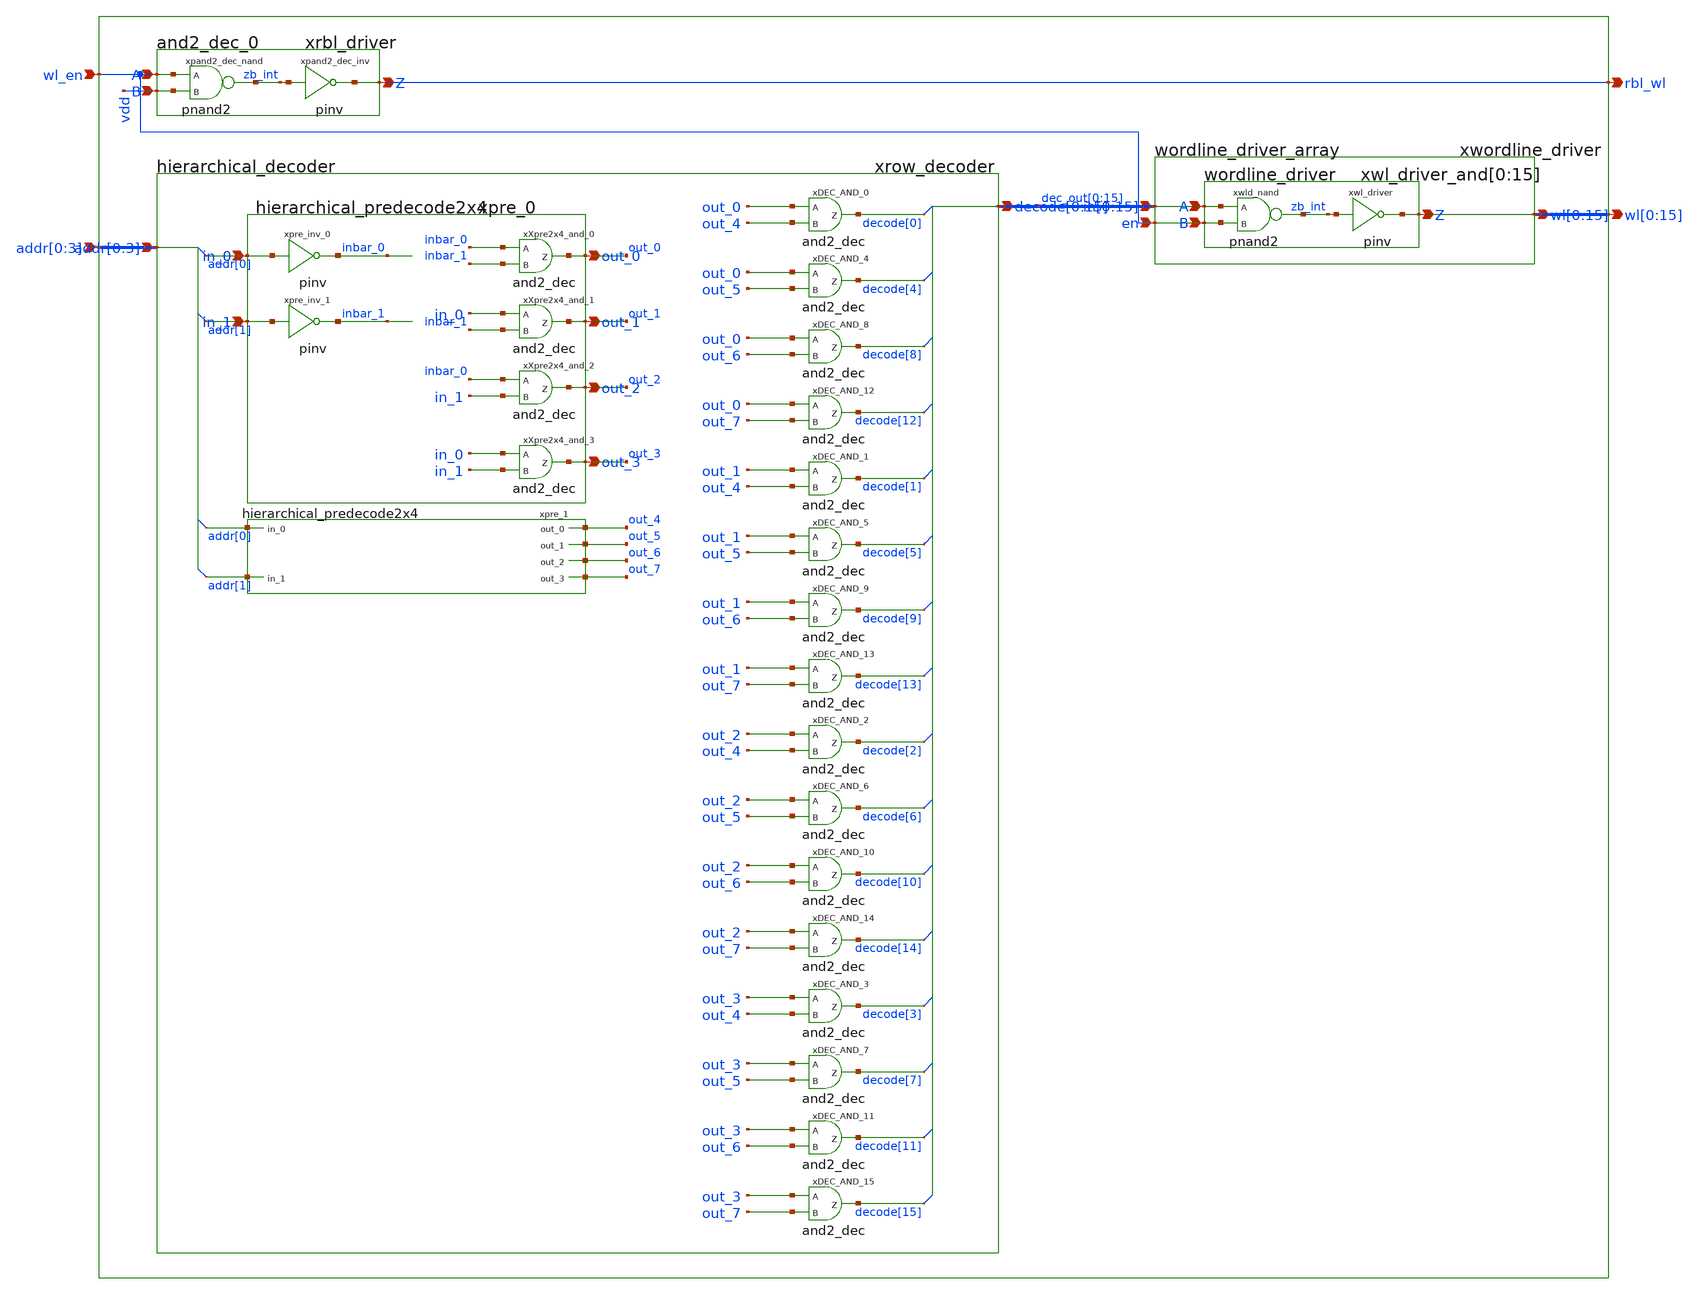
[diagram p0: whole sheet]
** sch_path: sram_4_16_scn4m/port_address.sch
**.subckt port_address addr[0],addr[1],addr[2],addr[3] wl_en
*+ wl[0],wl[1],wl[2],wl[3],wl[4],wl[5],wl[6],wl[7],wl[8],wl[9],wl[10],wl[11],wl[12],wl[13],wl[14],wl[15] rbl_wl
*.ipin addr[0],addr[1],addr[2],addr[3]
*.ipin wl_en
*.opin
*+ wl[0],wl[1],wl[2],wl[3],wl[4],wl[5],wl[6],wl[7],wl[8],wl[9],wl[10],wl[11],wl[12],wl[13],wl[14],wl[15]
*.opin rbl_wl
xrow_decoder addr[0] addr[1] addr[2] addr[3] dec_out[0] dec_out[1] dec_out[2] dec_out[3] dec_out[4]
+ dec_out[5] dec_out[6] dec_out[7] dec_out[8] dec_out[9] dec_out[10] dec_out[11] dec_out[12] dec_out[13]
+ dec_out[14] dec_out[15] vdd gnd hierarchical_decoder
xwordline_driver dec_out[0] dec_out[1] dec_out[2] dec_out[3] dec_out[4] dec_out[5] dec_out[6]
+ dec_out[7] dec_out[8] dec_out[9] dec_out[10] dec_out[11] dec_out[12] dec_out[13] dec_out[14] dec_out[15] wl[0]
+ wl[1] wl[2] wl[3] wl[4] wl[5] wl[6] wl[7] wl[8] wl[9] wl[10] wl[11] wl[12] wl[13] wl[14] wl[15] wl_en vdd
+ gnd wordline_driver_array
xrbl_driver wl_en vdd rbl_wl vdd gnd and2_dec_0
**.ends

* expanding   symbol:  hierarchical_decoder.sch # of pins=2
** sym_path: sram_4_16_scn4m/hierarchical_decoder.sch
** sch_path: sram_4_16_scn4m/hierarchical_decoder.sch
.subckt hierarchical_decoder addr[0] addr[1] addr[2] addr[3] decode[0] decode[1] decode[2] decode[3]
+ decode[4] decode[5] decode[6] decode[7] decode[8] decode[9] decode[10] decode[11] decode[12] decode[13]
+ decode[14] decode[15] vdd gnd
*.ipin addr[0],addr[1],addr[2],addr[3]
*.opin
*+ decode[0],decode[1],decode[2],decode[3],decode[4],decode[5],decode[6],decode[7],decode[8],decode[9],decode[10],decode[11],decode[12],decode[13],decode[14],decode[15]
xpre_0 addr[0] addr[1] out_0 out_1 out_2 out_3 vdd gnd hierarchical_predecode2x4
xpre_1 addr[0] addr[1] out_4 out_5 out_6 out_7 vdd gnd hierarchical_predecode2x4
xDEC_AND_0 out_0 out_4 decode[0] and2_dec
xDEC_AND_4 out_0 out_5 decode[4] and2_dec
xDEC_AND_8 out_0 out_6 decode[8] and2_dec
xDEC_AND_12 out_0 out_7 decode[12] and2_dec
xDEC_AND_1 out_1 out_4 decode[1] and2_dec
xDEC_AND_5 out_1 out_5 decode[5] and2_dec
xDEC_AND_9 out_1 out_6 decode[9] and2_dec
xDEC_AND_13 out_1 out_7 decode[13] and2_dec
xDEC_AND_2 out_2 out_4 decode[2] and2_dec
xDEC_AND_6 out_2 out_5 decode[6] and2_dec
xDEC_AND_10 out_2 out_6 decode[10] and2_dec
xDEC_AND_14 out_2 out_7 decode[14] and2_dec
xDEC_AND_3 out_3 out_4 decode[3] and2_dec
xDEC_AND_7 out_3 out_5 decode[7] and2_dec
xDEC_AND_11 out_3 out_6 decode[11] and2_dec
xDEC_AND_15 out_3 out_7 decode[15] and2_dec
.ends


* expanding   symbol:  wordline_driver_array.sch # of pins=3
** sym_path: sram_4_16_scn4m/wordline_driver_array.sch
** sch_path: sram_4_16_scn4m/wordline_driver_array.sch
.subckt wordline_driver_array in[0] in[1] in[2] in[3] in[4] in[5] in[6] in[7] in[8] in[9] in[10]
+ in[11] in[12] in[13] in[14] in[15] wl[0] wl[1] wl[2] wl[3] wl[4] wl[5] wl[6] wl[7] wl[8] wl[9] wl[10]
+ wl[11] wl[12] wl[13] wl[14] wl[15] en vdd gnd
*.ipin
*+ in[0],in[1],in[2],in[3],in[4],in[5],in[6],in[7],in[8],in[9],in[10],in[11],in[12],in[13],in[14],in[15]
*.opin
*+ wl[0],wl[1],wl[2],wl[3],wl[4],wl[5],wl[6],wl[7],wl[8],wl[9],wl[10],wl[11],wl[12],wl[13],wl[14],wl[15]
*.ipin en
xwl_driver_and[0] in[0] en wl[0] vdd gnd wordline_driver
xwl_driver_and[1] in[1] en wl[1] vdd gnd wordline_driver
xwl_driver_and[2] in[2] en wl[2] vdd gnd wordline_driver
xwl_driver_and[3] in[3] en wl[3] vdd gnd wordline_driver
xwl_driver_and[4] in[4] en wl[4] vdd gnd wordline_driver
xwl_driver_and[5] in[5] en wl[5] vdd gnd wordline_driver
xwl_driver_and[6] in[6] en wl[6] vdd gnd wordline_driver
xwl_driver_and[7] in[7] en wl[7] vdd gnd wordline_driver
xwl_driver_and[8] in[8] en wl[8] vdd gnd wordline_driver
xwl_driver_and[9] in[9] en wl[9] vdd gnd wordline_driver
xwl_driver_and[10] in[10] en wl[10] vdd gnd wordline_driver
xwl_driver_and[11] in[11] en wl[11] vdd gnd wordline_driver
xwl_driver_and[12] in[12] en wl[12] vdd gnd wordline_driver
xwl_driver_and[13] in[13] en wl[13] vdd gnd wordline_driver
xwl_driver_and[14] in[14] en wl[14] vdd gnd wordline_driver
xwl_driver_and[15] in[15] en wl[15] vdd gnd wordline_driver
.ends


* expanding   symbol:  and2_dec_0.sch # of pins=3
** sym_path: sram_4_16_scn4m/and2_dec_0.sch
** sch_path: sram_4_16_scn4m/and2_dec_0.sch
.subckt and2_dec_0 A B Z vdd gnd
*.ipin A
*.ipin B
*.opin Z
xpand2_dec_nand A B zb_int vdd gnd pnand2
xpand2_dec_inv zb_int Z vdd gnd pinv
.ends


* expanding   symbol:  hierarchical_predecode2x4.sch # of pins=6
** sym_path: sram_4_16_scn4m/hierarchical_predecode2x4.sch
** sch_path: sram_4_16_scn4m/hierarchical_predecode2x4.sch
.subckt hierarchical_predecode2x4 in_0 in_1 out_0 out_1 out_2 out_3 vdd gnd
*.ipin in_0
*.ipin in_1
*.opin out_0
*.opin out_1
*.opin out_2
*.opin out_3
xpre_inv_0 in_0 inbar_0 vdd gnd pinv
xpre_inv_1 in_1 inbar_1 vdd gnd pinv
xXpre2x4_and_0 inbar_0 inbar_1 out_0 and2_dec
xXpre2x4_and_1 in_0 inbar_1 out_1 and2_dec
xXpre2x4_and_2 inbar_0 in_1 out_2 and2_dec
xXpre2x4_and_3 in_0 in_1 out_3 and2_dec
.ends


* expanding   symbol:  and2_dec.sym # of pins=3
** sym_path: sram_4_16_scn4m/and2_dec.sym
** sch_path: sram_4_16_scn4m/and2_dec.sch
.subckt and2_dec A B Z
*.ipin A
*.ipin B
*.opin Z
xpand2_dec_nand A B zb_int vdd gnd pnand2
xpand2_dec_inv zb_int Z vdd gnd pinv
.ends


* expanding   symbol:  wordline_driver.sch # of pins=3
** sym_path: sram_4_16_scn4m/wordline_driver.sch
** sch_path: sram_4_16_scn4m/wordline_driver.sch
.subckt wordline_driver A B Z vdd gnd
*.ipin A
*.ipin B
*.opin Z
xwld_nand A B zb_int vdd gnd pnand2
xwl_driver zb_int Z vdd gnd pinv
.ends


* expanding   symbol:  pnand2.sym # of pins=3
** sym_path: sram_2_64_scn4m/pnand2.sym
** sch_path: sram_2_64_scn4m/pnand2.sch
.subckt pnand2 A B Z vdd gnd
*.ipin A
*.ipin B
*.opin Z
*.iopin vdd
*.iopin gnd
XMpnand2_nmos1 Z B net1 gnd sky130_fd_pr__nfet_01v8 L=0.4 W=1.6 nf=1 ad='int((nf+1)/2) * W/nf * 0.29'
+ as='int((nf+2)/2) * W/nf * 0.29' pd='2*int((nf+1)/2) * (W/nf + 0.29)' ps='2*int((nf+2)/2) * (W/nf + 0.29)'
+ nrd='0.29 / W' nrs='0.29 / W' sa=0 sb=0 sd=0 mult=1 m=1
XMpnand2_pmos1 Z A vdd vdd sky130_fd_pr__pfet_01v8 L=0.4 W=1.6 nf=1 ad='int((nf+1)/2) * W/nf * 0.29'
+ as='int((nf+2)/2) * W/nf * 0.29' pd='2*int((nf+1)/2) * (W/nf + 0.29)' ps='2*int((nf+2)/2) * (W/nf + 0.29)'
+ nrd='0.29 / W' nrs='0.29 / W' sa=0 sb=0 sd=0 mult=1 m=1
XMpnand2_pmos2 Z B vdd vdd sky130_fd_pr__pfet_01v8 L=0.4 W=1.6 nf=1 ad='int((nf+1)/2) * W/nf * 0.29'
+ as='int((nf+2)/2) * W/nf * 0.29' pd='2*int((nf+1)/2) * (W/nf + 0.29)' ps='2*int((nf+2)/2) * (W/nf + 0.29)'
+ nrd='0.29 / W' nrs='0.29 / W' sa=0 sb=0 sd=0 mult=1 m=1
XMpnand2_nmos2 net1 A gnd gnd sky130_fd_pr__nfet_01v8 L=0.4 W=1.6 nf=1 ad='int((nf+1)/2) * W/nf * 0.29'
+ as='int((nf+2)/2) * W/nf * 0.29' pd='2*int((nf+1)/2) * (W/nf + 0.29)' ps='2*int((nf+2)/2) * (W/nf + 0.29)'
+ nrd='0.29 / W' nrs='0.29 / W' sa=0 sb=0 sd=0 mult=1 m=1
.ends


* expanding   symbol:  pinv.sym # of pins=2
** sym_path: sram_4_16_scn4m/pinv.sym
** sch_path: sram_4_16_scn4m/pinv.sch
.subckt pinv A Z vdd gnd
*.ipin A
*.opin Z
XMpinv_nmos Z A gnd gnd sky130_fd_pr__nfet_01v8 L=0.4 W=0.8 nf=1 ad='int((nf+1)/2) * W/nf * 0.29' as='int((nf+2)/2) * W/nf * 0.29'
+ pd='2*int((nf+1)/2) * (W/nf + 0.29)' ps='2*int((nf+2)/2) * (W/nf + 0.29)' nrd='0.29 / W' nrs='0.29 / W'
+ sa=0 sb=0 sd=0 mult=1 m=1
XMp_inv_pmos Z A vdd vdd sky130_fd_pr__pfet_01v8 L=0.4 W=1.6 nf=1 ad='int((nf+1)/2) * W/nf * 0.29' as='int((nf+2)/2) * W/nf * 0.29'
+ pd='2*int((nf+1)/2) * (W/nf + 0.29)' ps='2*int((nf+2)/2) * (W/nf + 0.29)' nrd='0.29 / W' nrs='0.29 / W'
+ sa=0 sb=0 sd=0 mult=1 m=1
.ends

.end
